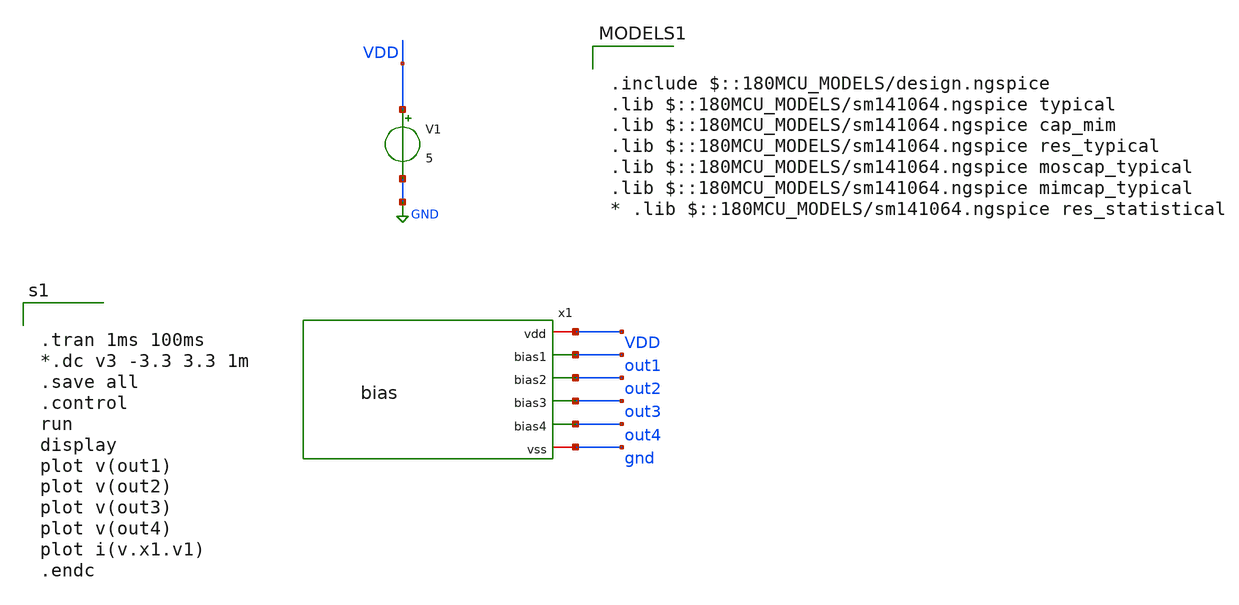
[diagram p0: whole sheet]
** sch_path: activities/opamp2AKAM/simulations_testbench/simulations_testbench/test_opam.sch
**.subckt test_opam
V1 VDD GND 5
x1 VDD out1 out2 out3 out4 gnd bias
**** begin user architecture code


.tran 1ms 100ms
*.dc v3 -3.3 3.3 1m
.save all
.control
run
display
plot v(out1)
plot v(out2)
plot v(out3)
plot v(out4)
plot i(v.x1.v1)
.endc



.include $::180MCU_MODELS/design.ngspice
.lib $::180MCU_MODELS/sm141064.ngspice typical
.lib $::180MCU_MODELS/sm141064.ngspice cap_mim
.lib $::180MCU_MODELS/sm141064.ngspice res_typical
.lib $::180MCU_MODELS/sm141064.ngspice moscap_typical
.lib $::180MCU_MODELS/sm141064.ngspice mimcap_typical
* .lib $::180MCU_MODELS/sm141064.ngspice res_statistical

**** end user architecture code
**.ends

* expanding   symbol:  DESIGN/AMPLIFIER/NEW/bias.sym # of pins=6
** sym_path: activities/opamp2AKAM/bias.sym
** sch_path: activities/opamp2AKAM/bias.sch
.subckt bias vdd bias1 bias2 bias3 bias4 vss
*.opin bias1
*.opin bias2
*.opin bias3
*.opin bias4
*.iopin vdd
*.iopin vss
XM4 net3 bias1 vdd vdd pfet_06v0 L=1.0u W=10.0u nf=1 ad='int((nf+1)/2) * W/nf * 0.18u' as='int((nf+2)/2) * W/nf * 0.18u'
+ pd='2*int((nf+1)/2) * (W/nf + 0.18u)' ps='2*int((nf+2)/2) * (W/nf + 0.18u)' nrd='0.18u / W' nrs='0.18u / W'
+ sa=0 sb=0 sd=0 m=1
XM5 bias3 bias2 net3 vdd pfet_06v0 L=1.0u W=10.0u nf=1 ad='int((nf+1)/2) * W/nf * 0.18u' as='int((nf+2)/2) * W/nf * 0.18u'
+ pd='2*int((nf+1)/2) * (W/nf + 0.18u)' ps='2*int((nf+2)/2) * (W/nf + 0.18u)' nrd='0.18u / W' nrs='0.18u / W'
+ sa=0 sb=0 sd=0 m=1
XM6 bias3 bias3 vss vss nfet_06v0 L=1.0u W=1.0u nf=1 ad='int((nf+1)/2) * W/nf * 0.18u' as='int((nf+2)/2) * W/nf * 0.18u'
+ pd='2*int((nf+1)/2) * (W/nf + 0.18u)' ps='2*int((nf+2)/2) * (W/nf + 0.18u)' nrd='0.18u / W' nrs='0.18u / W'
+ sa=0 sb=0 sd=0 m=1
XM7 net2 bias1 vdd vdd pfet_06v0 L=1.0u W=10.0u nf=1 ad='int((nf+1)/2) * W/nf * 0.18u' as='int((nf+2)/2) * W/nf * 0.18u'
+ pd='2*int((nf+1)/2) * (W/nf + 0.18u)' ps='2*int((nf+2)/2) * (W/nf + 0.18u)' nrd='0.18u / W' nrs='0.18u / W'
+ sa=0 sb=0 sd=0 m=1
XM8 bias4 bias2 net2 vdd pfet_06v0 L=1.0u W=10.0u nf=1 ad='int((nf+1)/2) * W/nf * 0.18u' as='int((nf+2)/2) * W/nf * 0.18u'
+ pd='2*int((nf+1)/2) * (W/nf + 0.18u)' ps='2*int((nf+2)/2) * (W/nf + 0.18u)' nrd='0.18u / W' nrs='0.18u / W'
+ sa=0 sb=0 sd=0 m=1
XM9 bias4 bias3 net1 vss nfet_06v0 L=1.0u W=5.0u nf=1 ad='int((nf+1)/2) * W/nf * 0.18u' as='int((nf+2)/2) * W/nf * 0.18u'
+ pd='2*int((nf+1)/2) * (W/nf + 0.18u)' ps='2*int((nf+2)/2) * (W/nf + 0.18u)' nrd='0.18u / W' nrs='0.18u / W'
+ sa=0 sb=0 sd=0 m=1
XM10 net1 bias4 vss vss nfet_06v0 L=1.0u W=5.0u nf=1 ad='int((nf+1)/2) * W/nf * 0.18u' as='int((nf+2)/2) * W/nf * 0.18u'
+ pd='2*int((nf+1)/2) * (W/nf + 0.18u)' ps='2*int((nf+2)/2) * (W/nf + 0.18u)' nrd='0.18u / W' nrs='0.18u / W'
+ sa=0 sb=0 sd=0 m=1
XM1 bias2 bias2 vdd vdd pfet_06v0 L=1.0u W=2u nf=1 ad='int((nf+1)/2) * W/nf * 0.18u' as='int((nf+2)/2) * W/nf * 0.18u'
+ pd='2*int((nf+1)/2) * (W/nf + 0.18u)' ps='2*int((nf+2)/2) * (W/nf + 0.18u)' nrd='0.18u / W' nrs='0.18u / W'
+ sa=0 sb=0 sd=0 m=1
XM2 net4 bias1 vdd vdd pfet_06v0 L=1.0u W=10.0u nf=1 ad='int((nf+1)/2) * W/nf * 0.18u' as='int((nf+2)/2) * W/nf * 0.18u'
+ pd='2*int((nf+1)/2) * (W/nf + 0.18u)' ps='2*int((nf+2)/2) * (W/nf + 0.18u)' nrd='0.18u / W' nrs='0.18u / W'
+ sa=0 sb=0 sd=0 m=1
XM3 bias1 bias2 net4 vdd pfet_06v0 L=1.0u W=10.0u nf=1 ad='int((nf+1)/2) * W/nf * 0.18u' as='int((nf+2)/2) * W/nf * 0.18u'
+ pd='2*int((nf+1)/2) * (W/nf + 0.18u)' ps='2*int((nf+2)/2) * (W/nf + 0.18u)' nrd='0.18u / W' nrs='0.18u / W'
+ sa=0 sb=0 sd=0 m=1
XM47 net5 bias2 vss vss nfet_06v0 L=1.0u W=1.0u nf=1 ad='int((nf+1)/2) * W/nf * 0.18u' as='int((nf+2)/2) * W/nf * 0.18u'
+ pd='2*int((nf+1)/2) * (W/nf + 0.18u)' ps='2*int((nf+2)/2) * (W/nf + 0.18u)' nrd='0.18u / W' nrs='0.18u / W'
+ sa=0 sb=0 sd=0 m=1
XM48 net6 bias2 vss vss nfet_06v0 L=1.0u W=1.0u nf=1 ad='int((nf+1)/2) * W/nf * 0.18u' as='int((nf+2)/2) * W/nf * 0.18u'
+ pd='2*int((nf+1)/2) * (W/nf + 0.18u)' ps='2*int((nf+2)/2) * (W/nf + 0.18u)' nrd='0.18u / W' nrs='0.18u / W'
+ sa=0 sb=0 sd=0 m=1
XM49 bias2 bias2 net6 vss nfet_06v0 L=1.0u W=1.0u nf=1 ad='int((nf+1)/2) * W/nf * 0.18u' as='int((nf+2)/2) * W/nf * 0.18u'
+ pd='2*int((nf+1)/2) * (W/nf + 0.18u)' ps='2*int((nf+2)/2) * (W/nf + 0.18u)' nrd='0.18u / W' nrs='0.18u / W'
+ sa=0 sb=0 sd=0 m=1
XM50 bias1 bias2 net5 vss nfet_06v0 L=1.0u W=1.0u nf=1 ad='int((nf+1)/2) * W/nf * 0.18u' as='int((nf+2)/2) * W/nf * 0.18u'
+ pd='2*int((nf+1)/2) * (W/nf + 0.18u)' ps='2*int((nf+2)/2) * (W/nf + 0.18u)' nrd='0.18u / W' nrs='0.18u / W'
+ sa=0 sb=0 sd=0 m=1
.ends

.GLOBAL GND
.end
